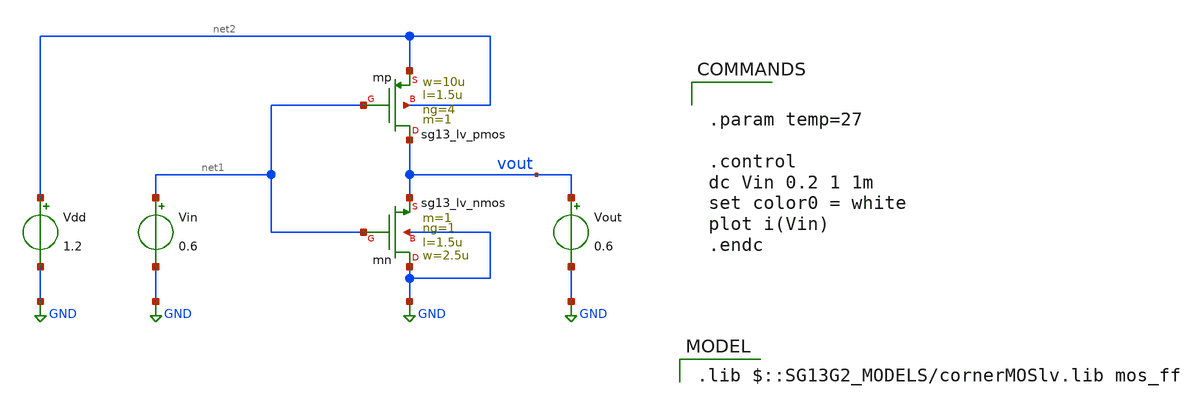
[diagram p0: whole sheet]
** sch_path: 5_Design/3_Real_circuits/sandbox_boris/tb_inv_leak.sch
**.subckt tb_inv_leak
Xmn GND net1 vout GND sg13_lv_nmos w=2.5u l=1.5u ng=1 m=1 mm_ok=1
Vin net1 GND 0.6
Xmp vout net1 net2 net2 sg13_lv_pmos w=10u l=1.5u ng=4 m=1 mm_ok=1
Vdd net2 GND 1.2
Vout vout GND 0.6
**** begin user architecture code
 .lib $::SG13G2_MODELS/cornerMOSlv.lib mos_ff



.param temp=27

.control
dc Vin 0.2 1 1m
set color0 = white
plot i(Vin)
.endc


**** end user architecture code
**.ends
.GLOBAL GND
.end
